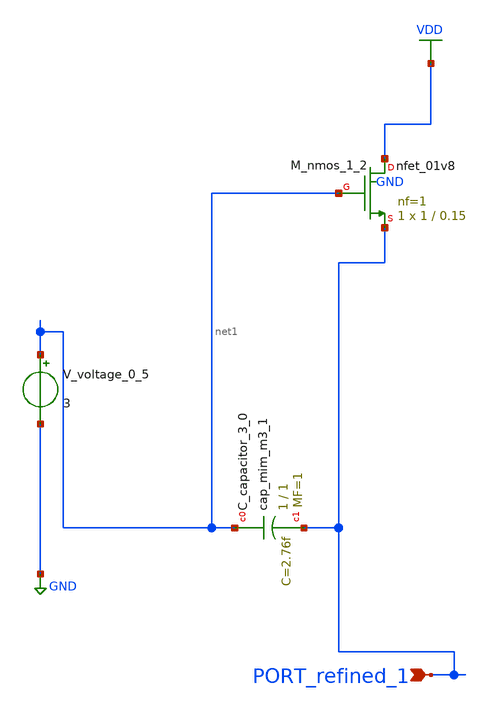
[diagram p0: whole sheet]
** sch_path: schematics/AMSNet/54.sch
**.subckt 54 PORT_refined_1
*.ipin PORT_refined_1
XC_capacitor_3_0 net1 PORT_refined_1 sky130_fd_pr__cap_mim_m3_1 W=1 L=1 MF=1 m=1
XM_nmos_1_2 VDD net1 PORT_refined_1 GND sky130_fd_pr__nfet_01v8 L=0.15 W=1 nf=1 ad='int((1 + 1)/2) * 1 / 1 * 0.29'
+ as='int((1 + 2)/2) * 1 / 1 * 0.29' pd='2*int((1 + 1)/2) * (1 / 1 + 0.29)' ps='2*int((1 + 2)/2) * (1 / 1 + 0.29)'
+ nrd='0.29 / 1 ' nrs='0.29 / 1 ' sa=0 sb=0 sd=0 mult=1 m=1
V_voltage_0_5 net1 GND 3
**.ends
.GLOBAL GND
.GLOBAL VDD
.end
